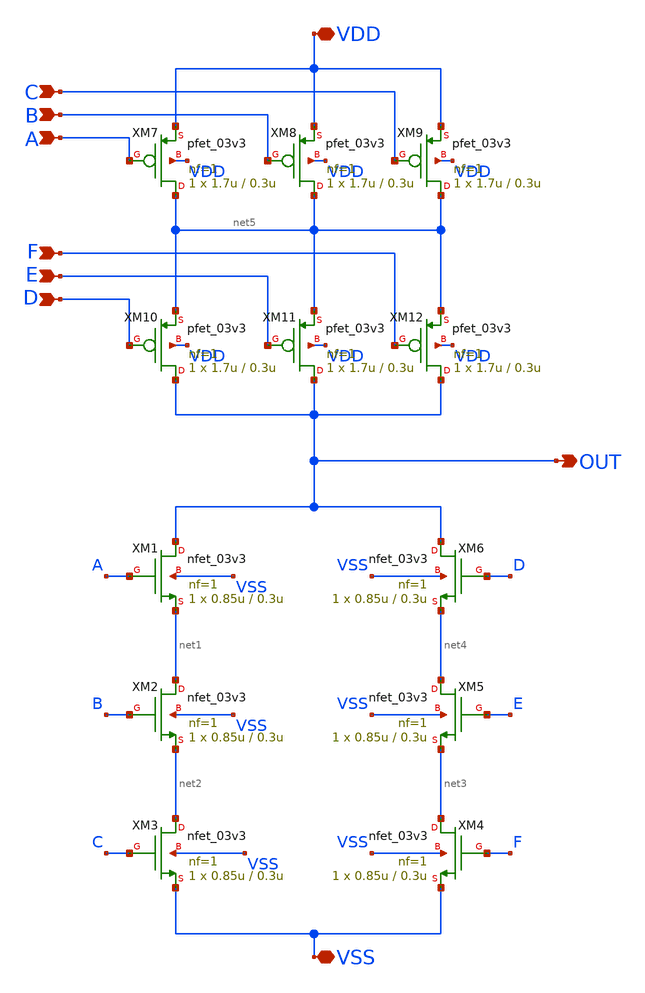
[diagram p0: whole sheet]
** sch_path: designs/AOI33/Pre_Layout/Schematic/gf180mcu_osu_sc_gp9t3v3__aoi33_1.sch
**.subckt gf180mcu_osu_sc_gp9t3v3__aoi33_1 VSS VDD A D E B C F OUT
*.iopin VSS
*.iopin VDD
*.ipin A
*.ipin D
*.ipin E
*.ipin B
*.ipin C
*.ipin F
*.opin OUT
XM1 OUT A net1 VSS nfet_03v3 L=0.3u W=0.85u nf=1 ad='int((nf+1)/2) * W/nf * 0.18u' as='int((nf+2)/2) * W/nf * 0.18u'
+ pd='2*int((nf+1)/2) * (W/nf + 0.18u)' ps='2*int((nf+2)/2) * (W/nf + 0.18u)' nrd='0.18u / W' nrs='0.18u / W'
+ sa=0 sb=0 sd=0 m=1
XM7 net5 A VDD VDD pfet_03v3 L=0.3u W=1.7u nf=1 ad='int((nf+1)/2) * W/nf * 0.18u' as='int((nf+2)/2) * W/nf * 0.18u'
+ pd='2*int((nf+1)/2) * (W/nf + 0.18u)' ps='2*int((nf+2)/2) * (W/nf + 0.18u)' nrd='0.18u / W' nrs='0.18u / W'
+ sa=0 sb=0 sd=0 m=1
XM8 net5 B VDD VDD pfet_03v3 L=0.3u W=1.7u nf=1 ad='int((nf+1)/2) * W/nf * 0.18u' as='int((nf+2)/2) * W/nf * 0.18u'
+ pd='2*int((nf+1)/2) * (W/nf + 0.18u)' ps='2*int((nf+2)/2) * (W/nf + 0.18u)' nrd='0.18u / W' nrs='0.18u / W'
+ sa=0 sb=0 sd=0 m=1
XM9 net5 C VDD VDD pfet_03v3 L=0.3u W=1.7u nf=1 ad='int((nf+1)/2) * W/nf * 0.18u' as='int((nf+2)/2) * W/nf * 0.18u'
+ pd='2*int((nf+1)/2) * (W/nf + 0.18u)' ps='2*int((nf+2)/2) * (W/nf + 0.18u)' nrd='0.18u / W' nrs='0.18u / W'
+ sa=0 sb=0 sd=0 m=1
XM10 OUT D net5 VDD pfet_03v3 L=0.3u W=1.7u nf=1 ad='int((nf+1)/2) * W/nf * 0.18u' as='int((nf+2)/2) * W/nf * 0.18u'
+ pd='2*int((nf+1)/2) * (W/nf + 0.18u)' ps='2*int((nf+2)/2) * (W/nf + 0.18u)' nrd='0.18u / W' nrs='0.18u / W'
+ sa=0 sb=0 sd=0 m=1
XM11 OUT E net5 VDD pfet_03v3 L=0.3u W=1.7u nf=1 ad='int((nf+1)/2) * W/nf * 0.18u' as='int((nf+2)/2) * W/nf * 0.18u'
+ pd='2*int((nf+1)/2) * (W/nf + 0.18u)' ps='2*int((nf+2)/2) * (W/nf + 0.18u)' nrd='0.18u / W' nrs='0.18u / W'
+ sa=0 sb=0 sd=0 m=1
XM12 OUT F net5 VDD pfet_03v3 L=0.3u W=1.7u nf=1 ad='int((nf+1)/2) * W/nf * 0.18u' as='int((nf+2)/2) * W/nf * 0.18u'
+ pd='2*int((nf+1)/2) * (W/nf + 0.18u)' ps='2*int((nf+2)/2) * (W/nf + 0.18u)' nrd='0.18u / W' nrs='0.18u / W'
+ sa=0 sb=0 sd=0 m=1
XM2 net1 B net2 VSS nfet_03v3 L=0.3u W=0.85u nf=1 ad='int((nf+1)/2) * W/nf * 0.18u' as='int((nf+2)/2) * W/nf * 0.18u'
+ pd='2*int((nf+1)/2) * (W/nf + 0.18u)' ps='2*int((nf+2)/2) * (W/nf + 0.18u)' nrd='0.18u / W' nrs='0.18u / W'
+ sa=0 sb=0 sd=0 m=1
XM3 net2 C VSS VSS nfet_03v3 L=0.3u W=0.85u nf=1 ad='int((nf+1)/2) * W/nf * 0.18u' as='int((nf+2)/2) * W/nf * 0.18u'
+ pd='2*int((nf+1)/2) * (W/nf + 0.18u)' ps='2*int((nf+2)/2) * (W/nf + 0.18u)' nrd='0.18u / W' nrs='0.18u / W'
+ sa=0 sb=0 sd=0 m=1
XM4 net3 F VSS VSS nfet_03v3 L=0.3u W=0.85u nf=1 ad='int((nf+1)/2) * W/nf * 0.18u' as='int((nf+2)/2) * W/nf * 0.18u'
+ pd='2*int((nf+1)/2) * (W/nf + 0.18u)' ps='2*int((nf+2)/2) * (W/nf + 0.18u)' nrd='0.18u / W' nrs='0.18u / W'
+ sa=0 sb=0 sd=0 m=1
XM5 net4 E net3 VSS nfet_03v3 L=0.3u W=0.85u nf=1 ad='int((nf+1)/2) * W/nf * 0.18u' as='int((nf+2)/2) * W/nf * 0.18u'
+ pd='2*int((nf+1)/2) * (W/nf + 0.18u)' ps='2*int((nf+2)/2) * (W/nf + 0.18u)' nrd='0.18u / W' nrs='0.18u / W'
+ sa=0 sb=0 sd=0 m=1
XM6 OUT D net4 VSS nfet_03v3 L=0.3u W=0.85u nf=1 ad='int((nf+1)/2) * W/nf * 0.18u' as='int((nf+2)/2) * W/nf * 0.18u'
+ pd='2*int((nf+1)/2) * (W/nf + 0.18u)' ps='2*int((nf+2)/2) * (W/nf + 0.18u)' nrd='0.18u / W' nrs='0.18u / W'
+ sa=0 sb=0 sd=0 m=1
**.ends
.end
